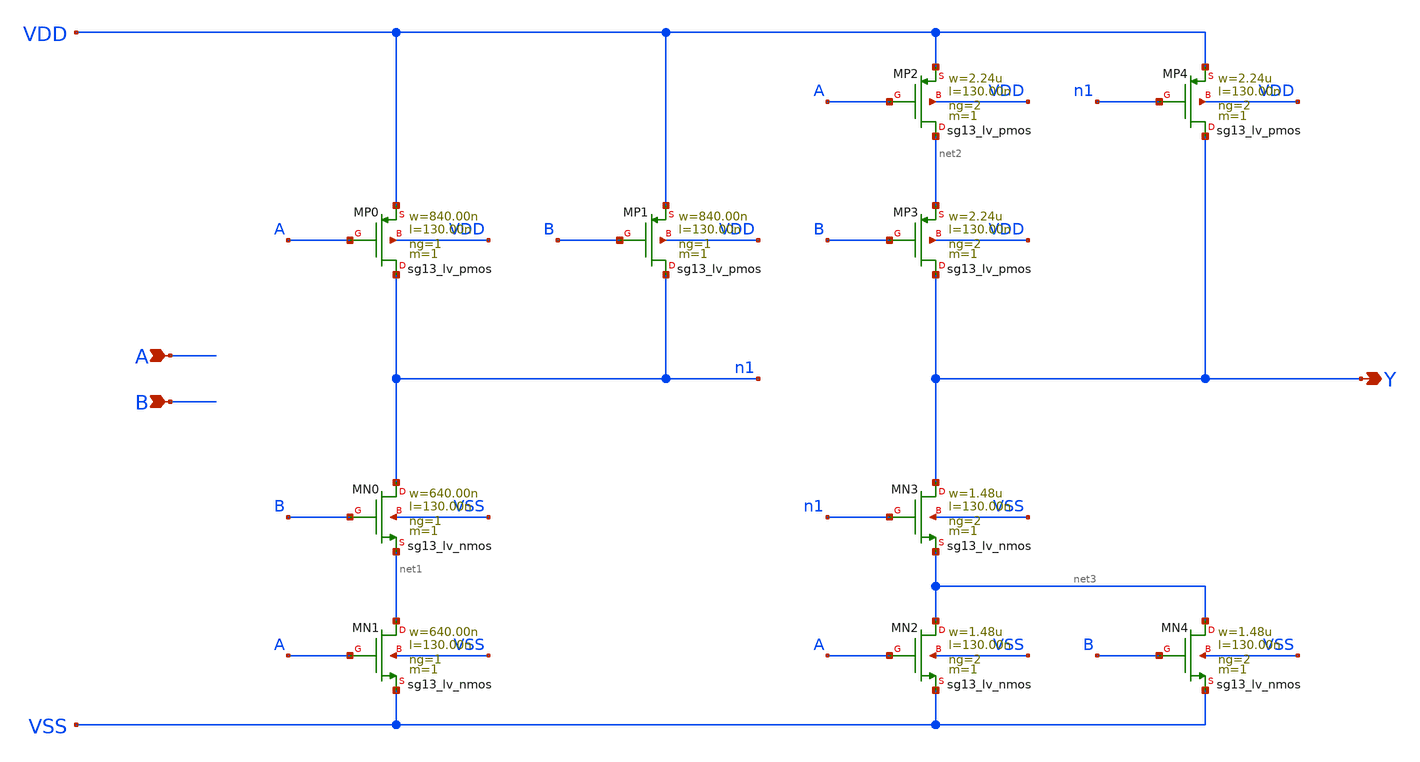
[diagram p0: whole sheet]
** sch_path: outputs/sg13g2_cells/cells/sg13g2_xnor2_2/sg13g2_xnor2_2.sch
**.subckt sg13g2_xnor2_2 A B Y
*.ipin A
*.ipin B
*.opin Y
XMN2 net3 A VSS VSS sg13_lv_nmos w=1.48u l=130.00n ng=2 m=1 mm_ok=1
XMN4 net3 B VSS VSS sg13_lv_nmos w=1.48u l=130.00n ng=2 m=1 mm_ok=1
XMN3 Y n1 net3 VSS sg13_lv_nmos w=1.48u l=130.00n ng=2 m=1 mm_ok=1
XMN0 n1 B net1 VSS sg13_lv_nmos w=640.00n l=130.00n ng=1 m=1 mm_ok=1
XMN1 net1 A VSS VSS sg13_lv_nmos w=640.00n l=130.00n ng=1 m=1 mm_ok=1
XMP0 n1 A VDD VDD sg13_lv_pmos w=840.00n l=130.00n ng=1 m=1 mm_ok=1
XMP1 n1 B VDD VDD sg13_lv_pmos w=840.00n l=130.00n ng=1 m=1 mm_ok=1
XMP2 net2 A VDD VDD sg13_lv_pmos w=2.24u l=130.00n ng=2 m=1 mm_ok=1
XMP3 Y B net2 VDD sg13_lv_pmos w=2.24u l=130.00n ng=2 m=1 mm_ok=1
XMP4 Y n1 VDD VDD sg13_lv_pmos w=2.24u l=130.00n ng=2 m=1 mm_ok=1
**.ends
.end
